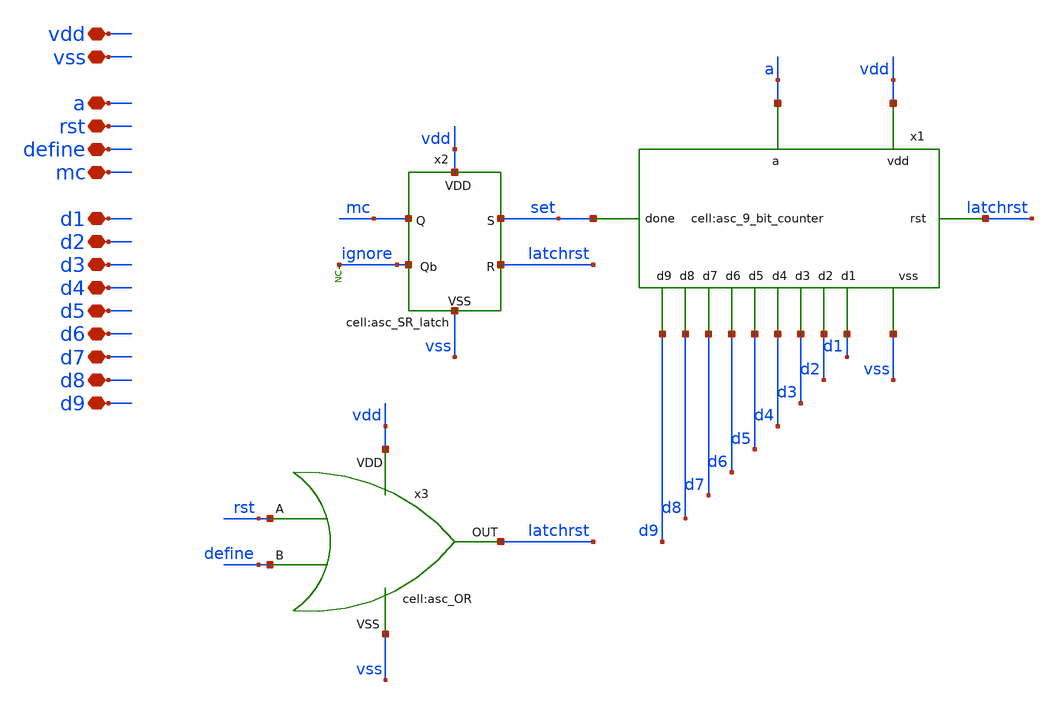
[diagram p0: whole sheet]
** sch_path: designs/libs/core_analog/asc_swallow_counter_20250721/asc_swallow_counter_20250721.sch
**.subckt asc_swallow_counter_20250721 vdd vss rst a mc d2 d1 d3 d5 d4 d6 d8 d7 d9 define
*.iopin vdd
*.iopin vss
*.iopin rst
*.iopin a
*.iopin mc
*.iopin d2
*.iopin d1
*.iopin d3
*.iopin d5
*.iopin d4
*.iopin d6
*.iopin d8
*.iopin d7
*.iopin d9
*.iopin define
x2 latchrst set ignore vdd vss mc asc_SR_latch
x3 vdd vss latchrst rst define asc_OR
x1 set d9 d8 d7 d6 d5 d4 d3 d2 d1 vss latchrst vdd a asc_9_bit_counter
* noconn ignore
**.ends
.end
